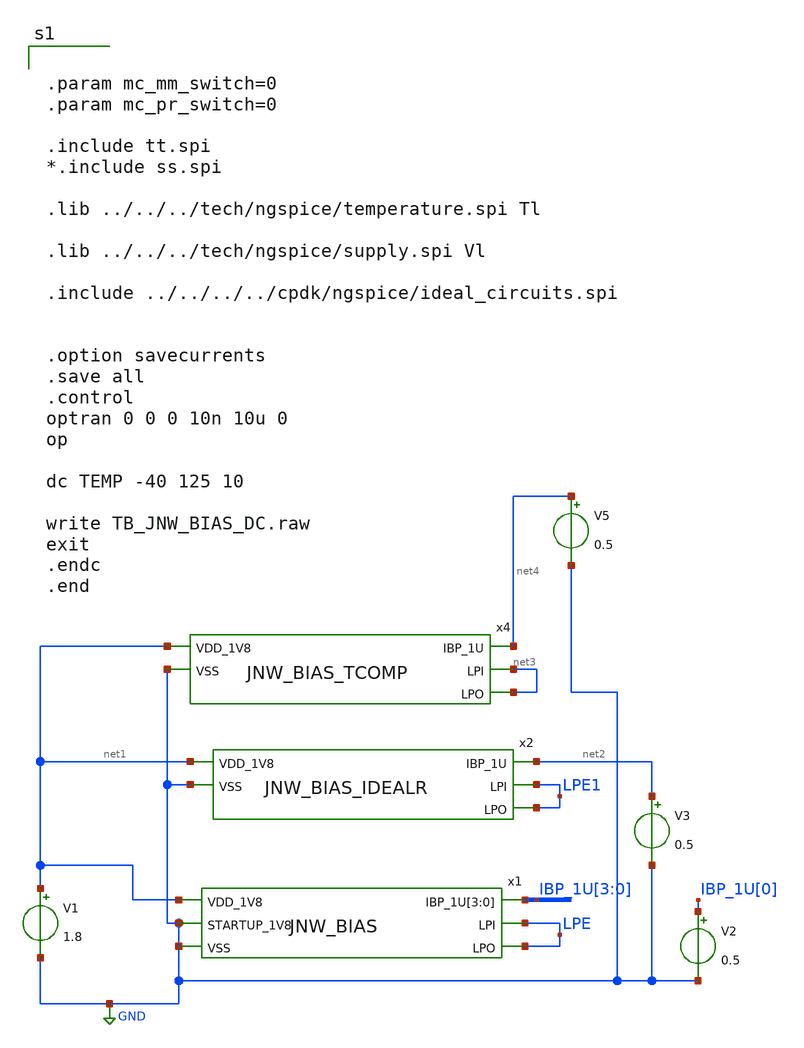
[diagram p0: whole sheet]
** sch_path: design/JNW_BIAS_SKY130A/TB_JNW_BIAS_DC.sch
**.subckt TB_JNW_BIAS_DC
x1 net1 LPE IBP_1U[3] IBP_1U[2] IBP_1U[1] IBP_1U[0] LPE GND GND JNW_BIAS
V1 net1 GND 1.8
V2 IBP_1U[0] GND 0.5
x2 net1 net2 LPE1 LPE1 GND JNW_BIAS_IDEALR
V3 net2 GND 0.5
x4 net1 net4 net3 net3 GND JNW_BIAS_TCOMP
V5 net4 GND 0.5
**** begin user architecture code


.param mc_mm_switch=0
.param mc_pr_switch=0

.include tt.spi
*.include ss.spi

.lib ../../../tech/ngspice/temperature.spi Tl

.lib ../../../tech/ngspice/supply.spi Vl

.include ../../../../cpdk/ngspice/ideal_circuits.spi


.option savecurrents
.save all
.control
optran 0 0 0 10n 10u 0
op

dc TEMP -40 125 10

write TB_JNW_BIAS_DC.raw
exit
.endc
.end



**** end user architecture code
**.ends
.GLOBAL GND
.end
